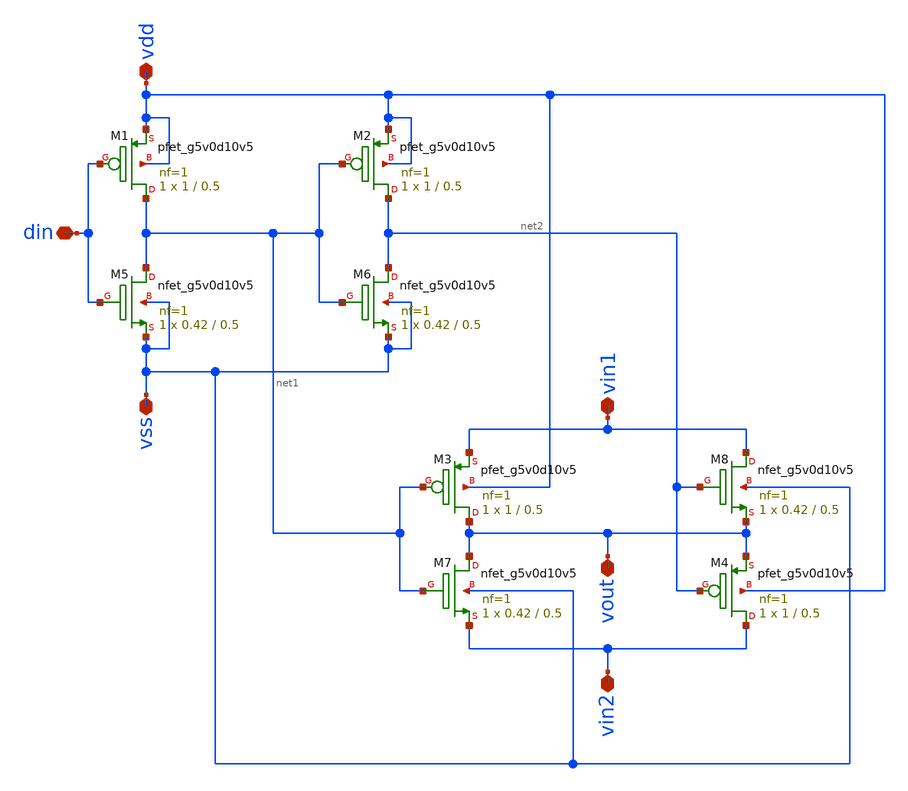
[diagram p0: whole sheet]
** sch_path: dac5v/1.schematics/sw.sch
**.subckt sw vdd vss din vin1 vin2 vout
*.iopin vdd
*.iopin vss
*.iopin din
*.iopin vin1
*.iopin vin2
*.iopin vout
XM2 net2 net1 vdd vdd sky130_fd_pr__pfet_g5v0d10v5 L=0.5 W=1 nf=1 ad='int((nf+1)/2) * W/nf * 0.29' as='int((nf+2)/2) * W/nf * 0.29'
+ pd='2*int((nf+1)/2) * (W/nf + 0.29)' ps='2*int((nf+2)/2) * (W/nf + 0.29)' nrd='0.29 / W' nrs='0.29 / W'
+ sa=0 sb=0 sd=0 mult=1 m=1
XM1 net1 din vdd vdd sky130_fd_pr__pfet_g5v0d10v5 L=0.5 W=1 nf=1 ad='int((nf+1)/2) * W/nf * 0.29' as='int((nf+2)/2) * W/nf * 0.29'
+ pd='2*int((nf+1)/2) * (W/nf + 0.29)' ps='2*int((nf+2)/2) * (W/nf + 0.29)' nrd='0.29 / W' nrs='0.29 / W'
+ sa=0 sb=0 sd=0 mult=1 m=1
XM3 vout net1 vin1 vdd sky130_fd_pr__pfet_g5v0d10v5 L=0.5 W=1 nf=1 ad='int((nf+1)/2) * W/nf * 0.29' as='int((nf+2)/2) * W/nf * 0.29'
+ pd='2*int((nf+1)/2) * (W/nf + 0.29)' ps='2*int((nf+2)/2) * (W/nf + 0.29)' nrd='0.29 / W' nrs='0.29 / W'
+ sa=0 sb=0 sd=0 mult=1 m=1
XM4 vin2 net2 vout vdd sky130_fd_pr__pfet_g5v0d10v5 L=0.5 W=1 nf=1 ad='int((nf+1)/2) * W/nf * 0.29' as='int((nf+2)/2) * W/nf * 0.29'
+ pd='2*int((nf+1)/2) * (W/nf + 0.29)' ps='2*int((nf+2)/2) * (W/nf + 0.29)' nrd='0.29 / W' nrs='0.29 / W'
+ sa=0 sb=0 sd=0 mult=1 m=1
XM5 net1 din vss vss sky130_fd_pr__nfet_g5v0d10v5 L=0.5 W=0.42 nf=1 ad='int((nf+1)/2) * W/nf * 0.29'
+ as='int((nf+2)/2) * W/nf * 0.29' pd='2*int((nf+1)/2) * (W/nf + 0.29)' ps='2*int((nf+2)/2) * (W/nf + 0.29)'
+ nrd='0.29 / W' nrs='0.29 / W' sa=0 sb=0 sd=0 mult=1 m=1
XM6 net2 net1 vss vss sky130_fd_pr__nfet_g5v0d10v5 L=0.5 W=0.42 nf=1 ad='int((nf+1)/2) * W/nf * 0.29'
+ as='int((nf+2)/2) * W/nf * 0.29' pd='2*int((nf+1)/2) * (W/nf + 0.29)' ps='2*int((nf+2)/2) * (W/nf + 0.29)'
+ nrd='0.29 / W' nrs='0.29 / W' sa=0 sb=0 sd=0 mult=1 m=1
XM7 vout net1 vin2 vss sky130_fd_pr__nfet_g5v0d10v5 L=0.5 W=0.42 nf=1 ad='int((nf+1)/2) * W/nf * 0.29'
+ as='int((nf+2)/2) * W/nf * 0.29' pd='2*int((nf+1)/2) * (W/nf + 0.29)' ps='2*int((nf+2)/2) * (W/nf + 0.29)'
+ nrd='0.29 / W' nrs='0.29 / W' sa=0 sb=0 sd=0 mult=1 m=1
XM8 vin1 net2 vout vss sky130_fd_pr__nfet_g5v0d10v5 L=0.5 W=0.42 nf=1 ad='int((nf+1)/2) * W/nf * 0.29'
+ as='int((nf+2)/2) * W/nf * 0.29' pd='2*int((nf+1)/2) * (W/nf + 0.29)' ps='2*int((nf+2)/2) * (W/nf + 0.29)'
+ nrd='0.29 / W' nrs='0.29 / W' sa=0 sb=0 sd=0 mult=1 m=1
**.ends
.end
